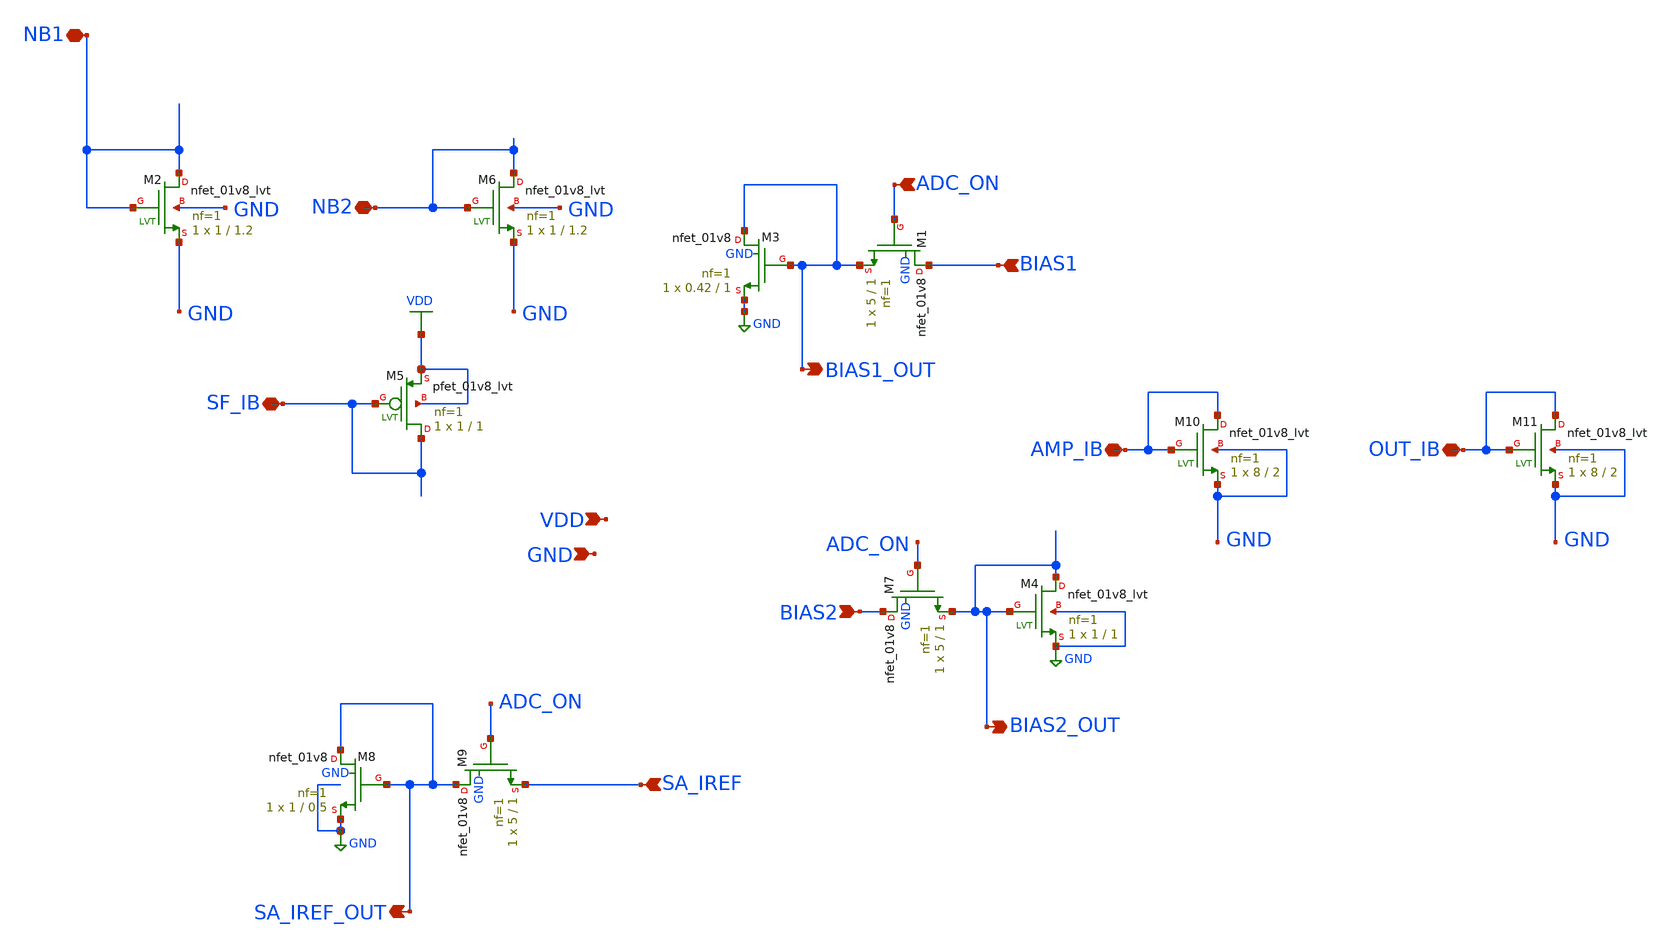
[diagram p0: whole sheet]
** sch_path: xschem/bias.sch
**.subckt bias SF_IB NB2 NB1 ADC_ON BIAS1 BIAS1_OUT BIAS2 BIAS2_OUT SA_IREF SA_IREF_OUT AMP_IB
*+ OUT_IB GND VDD
*.iopin SF_IB
*.iopin NB2
*.iopin NB1
*.ipin ADC_ON
*.ipin BIAS1
*.opin BIAS1_OUT
*.ipin BIAS2
*.opin BIAS2_OUT
*.ipin SA_IREF
*.opin SA_IREF_OUT
*.iopin AMP_IB
*.iopin OUT_IB
*.ipin GND
*.ipin VDD
XM2 NB1 NB1 GND GND sky130_fd_pr__nfet_01v8_lvt L=1.2 W=1 nf=1 ad='int((nf+1)/2) * W/nf * 0.29' as='int((nf+2)/2) * W/nf * 0.29'
+ pd='2*int((nf+1)/2) * (W/nf + 0.29)' ps='2*int((nf+2)/2) * (W/nf + 0.29)' nrd='0.29 / W' nrs='0.29 / W'
+ sa=0 sb=0 sd=0 mult=1 m=1
XM6 NB2 NB2 GND GND sky130_fd_pr__nfet_01v8_lvt L=1.2 W=1 nf=1 ad='int((nf+1)/2) * W/nf * 0.29' as='int((nf+2)/2) * W/nf * 0.29'
+ pd='2*int((nf+1)/2) * (W/nf + 0.29)' ps='2*int((nf+2)/2) * (W/nf + 0.29)' nrd='0.29 / W' nrs='0.29 / W'
+ sa=0 sb=0 sd=0 mult=1 m=1
XM3 BIAS1_OUT BIAS1_OUT GND GND sky130_fd_pr__nfet_01v8 L=1 W=0.42 nf=1 ad='int((nf+1)/2) * W/nf * 0.29'
+ as='int((nf+2)/2) * W/nf * 0.29' pd='2*int((nf+1)/2) * (W/nf + 0.29)' ps='2*int((nf+2)/2) * (W/nf + 0.29)'
+ nrd='0.29 / W' nrs='0.29 / W' sa=0 sb=0 sd=0 mult=1 m=1
XM4 BIAS2_OUT BIAS2_OUT GND GND sky130_fd_pr__nfet_01v8_lvt L=1 W=1 nf=1 ad='int((nf+1)/2) * W/nf * 0.29'
+ as='int((nf+2)/2) * W/nf * 0.29' pd='2*int((nf+1)/2) * (W/nf + 0.29)' ps='2*int((nf+2)/2) * (W/nf + 0.29)'
+ nrd='0.29 / W' nrs='0.29 / W' sa=0 sb=0 sd=0 mult=1 m=1
XM5 SF_IB SF_IB VDD VDD sky130_fd_pr__pfet_01v8_lvt L=1 W=1 nf=1 ad='int((nf+1)/2) * W/nf * 0.29' as='int((nf+2)/2) * W/nf * 0.29'
+ pd='2*int((nf+1)/2) * (W/nf + 0.29)' ps='2*int((nf+2)/2) * (W/nf + 0.29)' nrd='0.29 / W' nrs='0.29 / W'
+ sa=0 sb=0 sd=0 mult=1 m=1
XM1 BIAS1 ADC_ON BIAS1_OUT GND sky130_fd_pr__nfet_01v8 L=1 W=5 nf=1 ad='int((nf+1)/2) * W/nf * 0.29'
+ as='int((nf+2)/2) * W/nf * 0.29' pd='2*int((nf+1)/2) * (W/nf + 0.29)' ps='2*int((nf+2)/2) * (W/nf + 0.29)'
+ nrd='0.29 / W' nrs='0.29 / W' sa=0 sb=0 sd=0 mult=1 m=1
XM7 BIAS2 ADC_ON BIAS2_OUT GND sky130_fd_pr__nfet_01v8 L=1 W=5 nf=1 ad='int((nf+1)/2) * W/nf * 0.29'
+ as='int((nf+2)/2) * W/nf * 0.29' pd='2*int((nf+1)/2) * (W/nf + 0.29)' ps='2*int((nf+2)/2) * (W/nf + 0.29)'
+ nrd='0.29 / W' nrs='0.29 / W' sa=0 sb=0 sd=0 mult=1 m=1
XM9 SA_IREF_OUT ADC_ON SA_IREF GND sky130_fd_pr__nfet_01v8 L=1 W=5 nf=1 ad='int((nf+1)/2) * W/nf * 0.29'
+ as='int((nf+2)/2) * W/nf * 0.29' pd='2*int((nf+1)/2) * (W/nf + 0.29)' ps='2*int((nf+2)/2) * (W/nf + 0.29)'
+ nrd='0.29 / W' nrs='0.29 / W' sa=0 sb=0 sd=0 mult=1 m=1
XM10 AMP_IB AMP_IB GND GND sky130_fd_pr__nfet_01v8_lvt L=2 W=8 nf=1 ad='int((nf+1)/2) * W/nf * 0.29'
+ as='int((nf+2)/2) * W/nf * 0.29' pd='2*int((nf+1)/2) * (W/nf + 0.29)' ps='2*int((nf+2)/2) * (W/nf + 0.29)'
+ nrd='0.29 / W' nrs='0.29 / W' sa=0 sb=0 sd=0 mult=1 m=1
XM11 OUT_IB OUT_IB GND GND sky130_fd_pr__nfet_01v8_lvt L=2 W=8 nf=1 ad='int((nf+1)/2) * W/nf * 0.29'
+ as='int((nf+2)/2) * W/nf * 0.29' pd='2*int((nf+1)/2) * (W/nf + 0.29)' ps='2*int((nf+2)/2) * (W/nf + 0.29)'
+ nrd='0.29 / W' nrs='0.29 / W' sa=0 sb=0 sd=0 mult=1 m=1
XM8 SA_IREF_OUT SA_IREF_OUT GND GND sky130_fd_pr__nfet_01v8 L=0.5 W=1 nf=1 ad='int((nf+1)/2) * W/nf * 0.29'
+ as='int((nf+2)/2) * W/nf * 0.29' pd='2*int((nf+1)/2) * (W/nf + 0.29)' ps='2*int((nf+2)/2) * (W/nf + 0.29)'
+ nrd='0.29 / W' nrs='0.29 / W' sa=0 sb=0 sd=0 mult=1 m=1
**.ends
.GLOBAL GND
.GLOBAL VDD
.end
